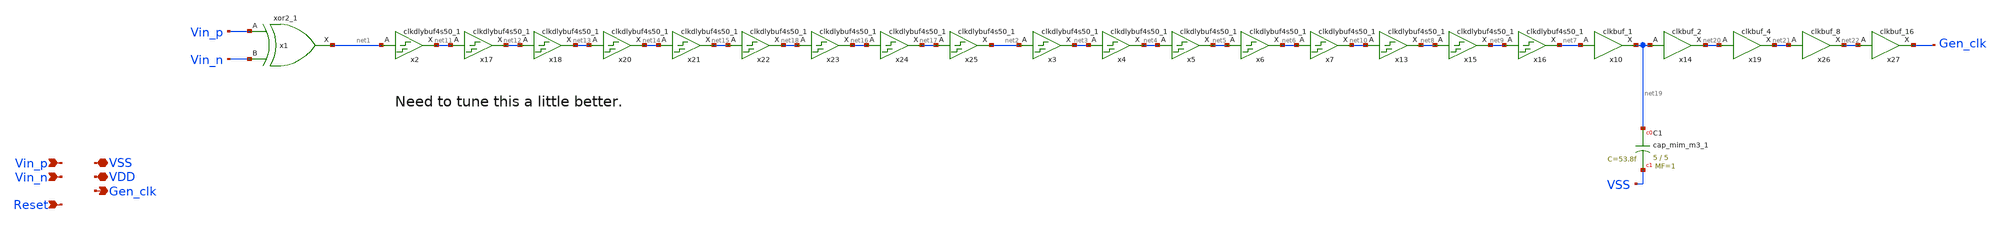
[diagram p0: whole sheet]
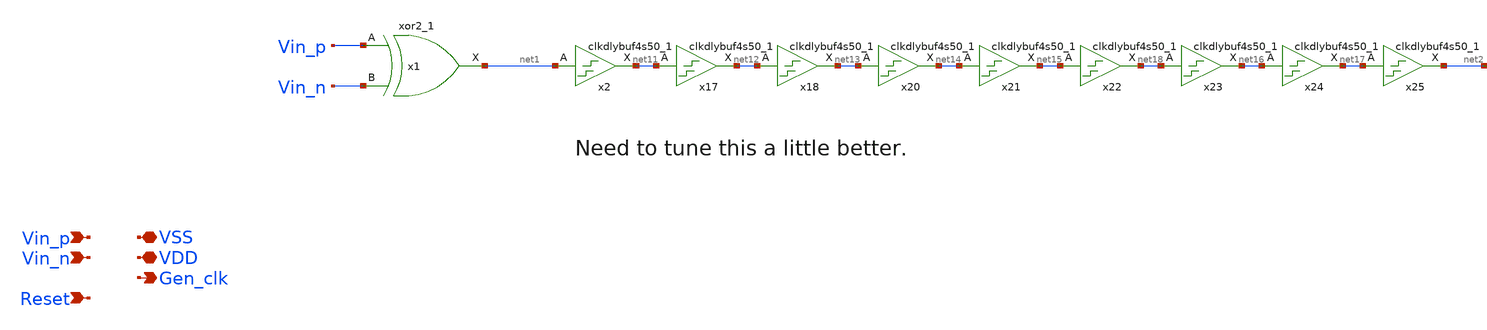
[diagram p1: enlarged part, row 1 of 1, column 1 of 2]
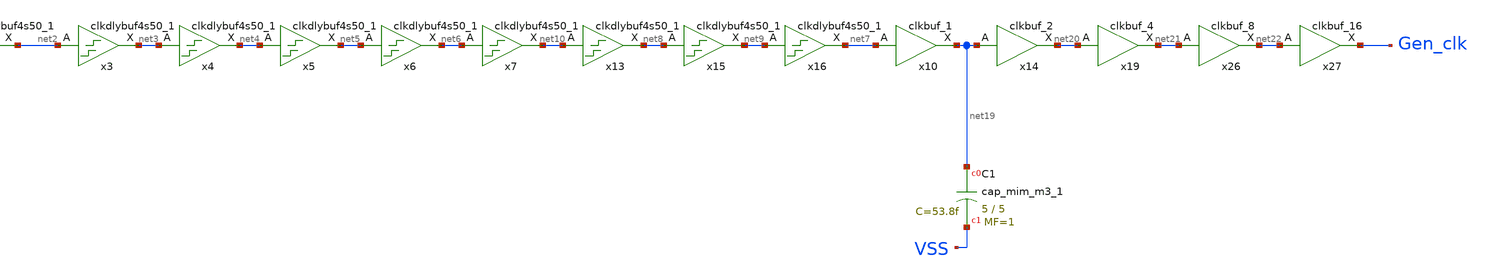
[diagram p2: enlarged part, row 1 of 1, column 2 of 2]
** sch_path: xschem/src/xor_clock_gen/xor_clock_gen_clkbuf_w_cap.sch
**.subckt xor_clock_gen_clkbuf_w_cap Vin_p VSS Gen_clk VDD Vin_n Reset
*.ipin Vin_p
*.iopin VSS
*.opin Gen_clk
*.iopin VDD
*.ipin Vin_n
*.ipin Reset
x1 Vin_p Vin_n VSS VSS VDD VDD net1 sky130_fd_sc_hd__xor2_1
x2 net1 VSS VSS VDD VDD net11 sky130_fd_sc_hd__clkdlybuf4s50_1
x3 net2 VSS VSS VDD VDD net3 sky130_fd_sc_hd__clkdlybuf4s50_1
x4 net3 VSS VSS VDD VDD net4 sky130_fd_sc_hd__clkdlybuf4s50_1
x5 net4 VSS VSS VDD VDD net5 sky130_fd_sc_hd__clkdlybuf4s50_1
x6 net5 VSS VSS VDD VDD net6 sky130_fd_sc_hd__clkdlybuf4s50_1
x7 net6 VSS VSS VDD VDD net10 sky130_fd_sc_hd__clkdlybuf4s50_1
x13 net10 VSS VSS VDD VDD net8 sky130_fd_sc_hd__clkdlybuf4s50_1
x15 net8 VSS VSS VDD VDD net9 sky130_fd_sc_hd__clkdlybuf4s50_1
x16 net9 VSS VSS VDD VDD net7 sky130_fd_sc_hd__clkdlybuf4s50_1
x17 net11 VSS VSS VDD VDD net12 sky130_fd_sc_hd__clkdlybuf4s50_1
x18 net12 VSS VSS VDD VDD net13 sky130_fd_sc_hd__clkdlybuf4s50_1
x20 net13 VSS VSS VDD VDD net14 sky130_fd_sc_hd__clkdlybuf4s50_1
x21 net14 VSS VSS VDD VDD net15 sky130_fd_sc_hd__clkdlybuf4s50_1
x22 net15 VSS VSS VDD VDD net18 sky130_fd_sc_hd__clkdlybuf4s50_1
x23 net18 VSS VSS VDD VDD net16 sky130_fd_sc_hd__clkdlybuf4s50_1
x24 net16 VSS VSS VDD VDD net17 sky130_fd_sc_hd__clkdlybuf4s50_1
x25 net17 VSS VSS VDD VDD net2 sky130_fd_sc_hd__clkdlybuf4s50_1
x10 net7 VSS VSS VDD VDD net19 sky130_fd_sc_hd__clkbuf_1
x14 net19 VSS VSS VDD VDD net20 sky130_fd_sc_hd__clkbuf_2
x19 net20 VSS VSS VDD VDD net21 sky130_fd_sc_hd__clkbuf_4
x26 net21 VSS VSS VDD VDD net22 sky130_fd_sc_hd__clkbuf_8
x27 net22 VSS VSS VDD VDD Gen_clk sky130_fd_sc_hd__clkbuf_16
XC1 net19 VSS sky130_fd_pr__cap_mim_m3_1 W=5 L=5 MF=1 m=1
**.ends
.end
